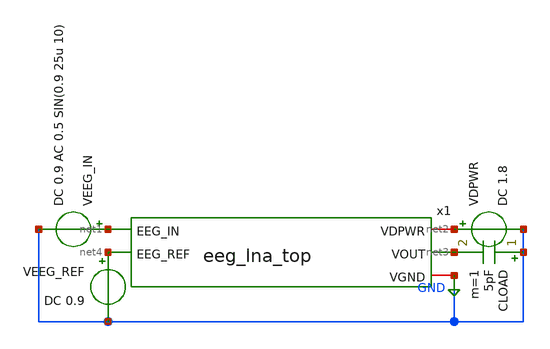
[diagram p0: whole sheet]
** sch_path: xschem/tb_eeg_lna_top.sch
**.subckt tb_eeg_lna_top
x1 net1 net2 net3 GND net4 eeg_lna_top
VDPWR net2 GND DC 1.8
VEEG_REF net4 GND DC 0.9
VEEG_IN net1 GND DC 0.9 AC 0.5 SIN(0.9 25u 10)
CLOAD GND net3 5pF m=1
**** begin user architecture code


.lib /foss/pdks/sky130A/libs.tech/ngspice/sky130.lib.spice tt

.ic v(net3)=0.5 v(x1.ota_inp)=0.5 v(x1.ota_inn)=0.5    v(x1.x_ota.tail_p)=1.5 v(x1.x_ota.net1)=0.5
+    v(x1.x_rpseudo_p.net1)=0.5 v(x1.x_rpseudo_fb.net1)=0.5

.nodeset v(net3)=0.5 v(x1.ota_inp)=0.5 v(x1.ota_inn)=0.5         v(x1.x_ota.tail_p)=1.5
+ v(x1.x_ota.net1)=0.5         v(x1.x_rpseudo_p.net1)=0.5 v(x1.x_rpseudo_fb.net1)=0.5

.option savecurrents

.control
op
echo ===== Bias Verification =====
print @m.x1.x_ota.xmtail[id]
print v(x1.x_ota.tail_p)
print v(x1.bias_p)
print @m.x1.x_ota.xmdiff_p[id]
print @m.x1.x_ota.xmdiff_n[id]

echo ===== Operating Point =====
print v(x1.ota_inp)
print v(x1.ota_inn)
print v(x1.ota_inp)-v(x1.ota_inn)
print v(net3)

echo ===== Transient =====
tran 1m 20 uic
plot v(net1)
plot v(x1.ota_inp)
plot v(x1.ota_inn)
plot v(x1.ota_inp)-v(x1.ota_inn)
plot v(net3)
plot v(net3)-0.84

echo ===== Noise =====
noise v(net3) veeg_in dec 100 0.5 100

* Active plot is the totals plot — print integrated values
print inoise_total
print onoise_total

* Switch to the spectrum plot to see vs frequency
setplot previous
plot db(inoise_spectrum)
plot db(onoise_spectrum)

echo ===== AC =====
ac dec 100 0.01 100k
plot db(v(net3)/v(net1))
.endc


**** end user architecture code
**.ends

* expanding   symbol:  eeg_lna_top.sym # of pins=5
** sym_path: xschem/eeg_lna_top.sym
** sch_path: xschem/eeg_lna_top.sch
.subckt eeg_lna_top EEG_IN VDPWR VOUT VGND EEG_REF
*.ipin EEG_IN
*.ipin EEG_REF
*.iopin VDPWR
*.iopin VGND
*.opin VOUT
XCIN_P EEG_IN OTA_INP sky130_fd_pr__cap_mim_m3_1 W=40 L=40 MF=1 m=1
XCIN_N EEG_REF OTA_INN sky130_fd_pr__cap_mim_m3_1 W=40 L=40 MF=1 m=1
x_ota BIAS_P VDPWR OTA_INP OTA_INN VOUT VGND ota_5t
x_rpseudo_p VDPWR VOUT OTA_INP pseudo_res_c
x_bias BIAS_P VGND VDPWR bias_gen
XCFB VOUT OTA_INN sky130_fd_pr__cap_mim_m3_1 W=20 L=20 MF=1 m=1
x_rpseudo_fb VDPWR OTA_INN VOUT pseudo_res_c
.ends


* expanding   symbol:  ota_5t.sym # of pins=6
** sym_path: xschem-new/ota_5t.sym
** sch_path: xschem-new/ota_5t.sch
.subckt ota_5t BIAS_P VDPWR VIN_P VIN_N VOUT VGND
*.ipin VIN_P
*.ipin VIN_N
*.ipin BIAS_P
*.iopin VDPWR
*.iopin VGND
*.opin VOUT
XMDIFF_P net1 VIN_P TAIL_P VDPWR sky130_fd_pr__pfet_01v8 L=4 W=48 nf=1 ad='int((1 + 1)/2) * 48 / 1 * 0.29'
+ as='int((1 + 2)/2) * 48 / 1 * 0.29' pd='2*int((1 + 1)/2) * (48 / 1 + 0.29)' ps='2*int((1 + 2)/2) * (48 / 1 + 0.29)'
+ nrd='0.29 / 48 ' nrs='0.29 / 48 ' sa=0 sb=0 sd=0 mult=1 m=1
XMDIFF_N VOUT VIN_N TAIL_P VDPWR sky130_fd_pr__pfet_01v8 L=4 W=48 nf=1 ad='int((1 + 1)/2) * 48 / 1 * 0.29'
+ as='int((1 + 2)/2) * 48 / 1 * 0.29' pd='2*int((1 + 1)/2) * (48 / 1 + 0.29)' ps='2*int((1 + 2)/2) * (48 / 1 + 0.29)'
+ nrd='0.29 / 48 ' nrs='0.29 / 48 ' sa=0 sb=0 sd=0 mult=1 m=1
XMTAIL TAIL_P BIAS_P VDPWR VDPWR sky130_fd_pr__pfet_01v8 L=8 W=0.5 nf=1 ad='int((1 + 1)/2) * 0.5 / 1 * 0.29'
+ as='int((1 + 2)/2) * 0.5 / 1 * 0.29' pd='2*int((1 + 1)/2) * (0.5 / 1 + 0.29)' ps='2*int((1 + 2)/2) * (0.5 / 1 + 0.29)'
+ nrd='0.29 / 0.5 ' nrs='0.29 / 0.5 ' sa=0 sb=0 sd=0 mult=1 m=1
XMLOAD_REF net1 net1 VGND VGND sky130_fd_pr__nfet_01v8 L=16 W=8 nf=1 ad='int((1 + 1)/2) * 8 / 1 * 0.29'
+ as='int((1 + 2)/2) * 8 / 1 * 0.29' pd='2*int((1 + 1)/2) * (8 / 1 + 0.29)' ps='2*int((1 + 2)/2) * (8 / 1 + 0.29)'
+ nrd='0.29 / 8 ' nrs='0.29 / 8 ' sa=0 sb=0 sd=0 mult=1 m=1
XMLOAD_OUT VOUT net1 VGND VGND sky130_fd_pr__nfet_01v8 L=16 W=8 nf=1 ad='int((1 + 1)/2) * 8 / 1 * 0.29'
+ as='int((1 + 2)/2) * 8 / 1 * 0.29' pd='2*int((1 + 1)/2) * (8 / 1 + 0.29)' ps='2*int((1 + 2)/2) * (8 / 1 + 0.29)'
+ nrd='0.29 / 8 ' nrs='0.29 / 8 ' sa=0 sb=0 sd=0 mult=1 m=1
.ends


* expanding   symbol:  pseudo_res_c.sym # of pins=3
** sym_path: xschem/pseudo_res_c.sym
** sch_path: xschem/pseudo_res_c.sch
.subckt pseudo_res_c VDPWR B A
*.iopin A
*.iopin B
*.iopin VDPWR
XP1 A net1 net1 VDPWR sky130_fd_pr__pfet_01v8 L=5 W=0.5 nf=1 ad='int((1 + 1)/2) * 0.5 / 1 * 0.29' as='int((1 + 2)/2) * 0.5 / 1 * 0.29'
+ pd='2*int((1 + 1)/2) * (0.5 / 1 + 0.29)' ps='2*int((1 + 2)/2) * (0.5 / 1 + 0.29)' nrd='0.29 / 0.5 ' nrs='0.29 / 0.5 '
+ sa=0 sb=0 sd=0 mult=10 m=10
XP2 net1 net1 B VDPWR sky130_fd_pr__pfet_01v8 L=5 W=0.5 nf=1 ad='int((1 + 1)/2) * 0.5 / 1 * 0.29' as='int((1 + 2)/2) * 0.5 / 1 * 0.29'
+ pd='2*int((1 + 1)/2) * (0.5 / 1 + 0.29)' ps='2*int((1 + 2)/2) * (0.5 / 1 + 0.29)' nrd='0.29 / 0.5 ' nrs='0.29 / 0.5 '
+ sa=0 sb=0 sd=0 mult=10 m=10
.ends


* expanding   symbol:  bias_gen.sym # of pins=3
** sym_path: xschem/bias_gen.sym
** sch_path: xschem/bias_gen.sch
.subckt bias_gen BIAS_P VGND VDPWR
*.iopin VDPWR
*.iopin VGND
*.opin BIAS_P
XM_BIAS_P BIAS_P BIAS_P VDPWR VDPWR sky130_fd_pr__pfet_01v8 L=2 W=1 nf=1 ad='int((1 + 1)/2) * 1 / 1 * 0.29'
+ as='int((1 + 2)/2) * 1 / 1 * 0.29' pd='2*int((1 + 1)/2) * (1 / 1 + 0.29)' ps='2*int((1 + 2)/2) * (1 / 1 + 0.29)'
+ nrd='0.29 / 1 ' nrs='0.29 / 1 ' sa=0 sb=0 sd=0 mult=1 m=1
XM_BIAS_N BIAS_P BIAS_P VGND VGND sky130_fd_pr__nfet_01v8 L=2 W=0.5 nf=1 ad='int((1 + 1)/2) * 0.5 / 1 * 0.29'
+ as='int((1 + 2)/2) * 0.5 / 1 * 0.29' pd='2*int((1 + 1)/2) * (0.5 / 1 + 0.29)' ps='2*int((1 + 2)/2) * (0.5 / 1 + 0.29)'
+ nrd='0.29 / 0.5 ' nrs='0.29 / 0.5 ' sa=0 sb=0 sd=0 mult=1 m=1
.ends

.GLOBAL GND
.end
